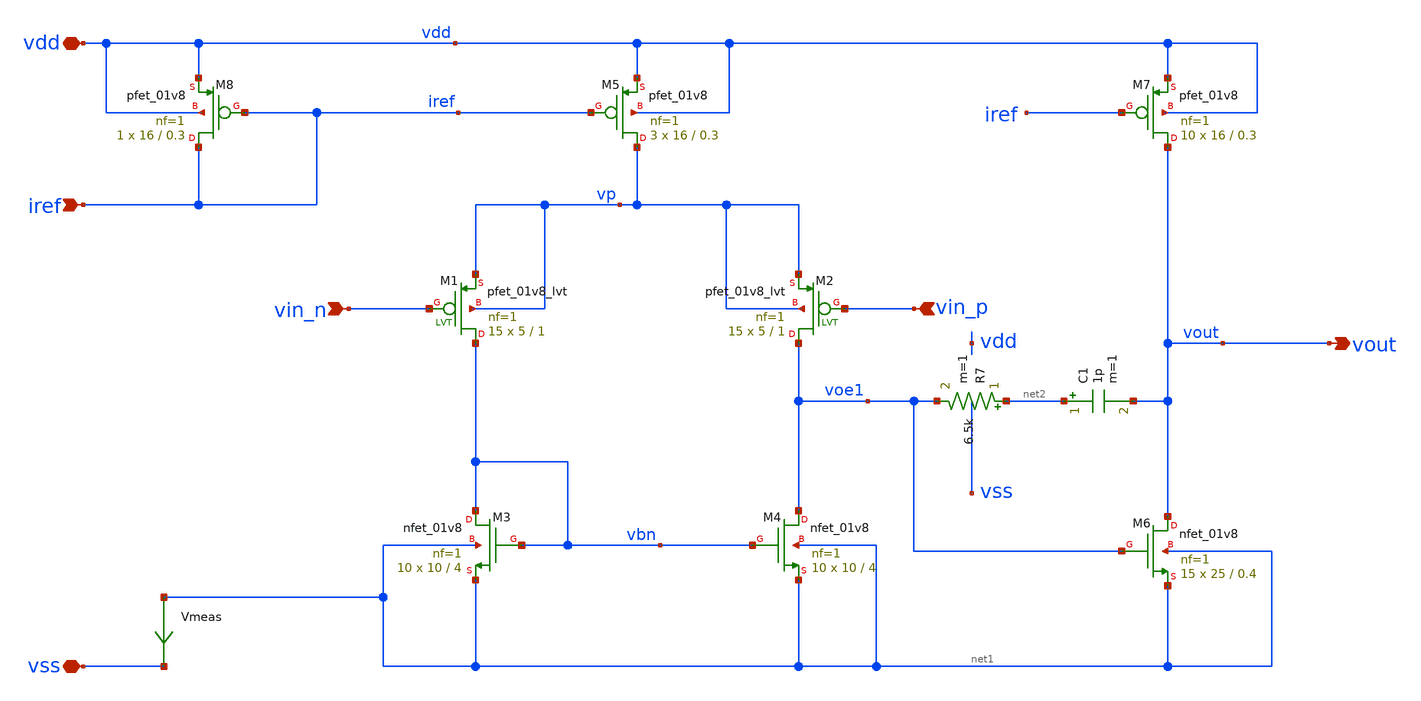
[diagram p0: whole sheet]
** sch_path: opamp/opamp.sch
**.subckt opamp vdd vss vin_n vin_p iref vout
*.iopin vdd
*.iopin vss
*.ipin vin_n
*.ipin vin_p
*.ipin iref
*.opin vout
XM3 vbn vbn net1 net1 sky130_fd_pr__nfet_01v8 L=4 W=10 nf=1 ad='W * 0.29' as='W * 0.29' pd='2 * (W + 0.29)'
+ ps='2 * (W + 0.29)' nrd='0.29 / W' nrs='0.29 / W' sa=0 sb=0 sd=0 mult=10 m=10
XM4 voe1 vbn net1 net1 sky130_fd_pr__nfet_01v8 L=4 W=10 nf=1 ad='W * 0.29' as='W * 0.29' pd='2 * (W + 0.29)'
+ ps='2 * (W + 0.29)' nrd='0.29 / W' nrs='0.29 / W' sa=0 sb=0 sd=0 mult=10 m=10
XM5 vp iref vdd vdd sky130_fd_pr__pfet_01v8 L=0.3 W=16 nf=1 ad='W * 0.29' as='W * 0.29' pd='2 * (W + 0.29)'
+ ps='2 * (W + 0.29)' nrd='0.29 / W' nrs='0.29 / W' sa=0 sb=0 sd=0 mult=3 m=3
XM7 vout iref vdd vdd sky130_fd_pr__pfet_01v8 L=0.3 W=16 nf=1 ad='W * 0.29' as='W * 0.29' pd='2 * (W + 0.29)'
+ ps='2 * (W + 0.29)' nrd='0.29 / W' nrs='0.29 / W' sa=0 sb=0 sd=0 mult=10 m=10
XM8 iref iref vdd vdd sky130_fd_pr__pfet_01v8 L=0.3 W=16 nf=1 ad='W * 0.29' as='W * 0.29' pd='2 * (W + 0.29)'
+ ps='2 * (W + 0.29)' nrd='0.29 / W' nrs='0.29 / W' sa=0 sb=0 sd=0 mult=1 m=1
XM6 vout voe1 net1 net1 sky130_fd_pr__nfet_01v8 L=0.4 W=25 nf=1 ad='W * 0.29' as='W * 0.29' pd='2 * (W + 0.29)'
+ ps='2 * (W + 0.29)' nrd='0.29 / W' nrs='0.29 / W' sa=0 sb=0 sd=0 mult=15 m=15
XM1 vbn vin_n vp vp sky130_fd_pr__pfet_01v8_lvt L=1 W=5 nf=1 ad='int((nf+1)/2) * W/nf * 0.29' as='int((nf+2)/2) * W/nf * 0.29'
+ pd='2*int((nf+1)/2) * (W/nf + 0.29)' ps='2*int((nf+2)/2) * (W/nf + 0.29)' nrd='0.29 / W' nrs='0.29 / W'
+ sa=0 sb=0 sd=0 mult=15 m=15
XM2 voe1 vin_p vp vp sky130_fd_pr__pfet_01v8_lvt L=1 W=5 nf=1 ad='int((nf+1)/2) * W/nf * 0.29' as='int((nf+2)/2) * W/nf * 0.29'
+ pd='2*int((nf+1)/2) * (W/nf + 0.29)' ps='2*int((nf+2)/2) * (W/nf + 0.29)' nrd='0.29 / W' nrs='0.29 / W'
+ sa=0 sb=0 sd=0 mult=15 m=15
C1 net2 vout 1p m=1
Vmeas net1 vss 0
.save i(vmeas)
R7 net2 voe1 6.5k m=1
**.ends
.end
